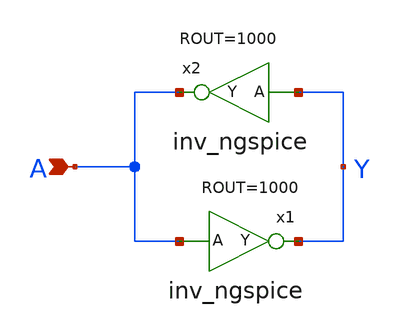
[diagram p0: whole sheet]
** sch_path: xschem_libs_newsym/ngspice/keeper_ngspice/schematic/keeper_ngspice.sch
* Copyright (C) 1998-2024 Stefan Frederik Schippers
* This program is free software; you can redistribute it and/or modify
* it under the terms of the GNU General Public License as published by
* the Free Software Foundation; either version 2 of the License, or
* (at your option) any later version.
* This program is distributed in the hope that it will be useful,
* but WITHOUT ANY WARRANTY; without even the implied warranty of
* MERCHANTABILITY or FITNESS FOR A PARTICULAR PURPOSE.  See the
* GNU General Public License for more details.
* You should have received a copy of the GNU General Public License
* along with this program; if not, write to the Free Software
**.subckt keeper_ngspice A
*.ipin A
x1 Y A inv_ngspice ROUT=1000
x2 A Y inv_ngspice ROUT=1000
**.ends

* expanding   symbol:  ngspice/inv_ngspice.sym # of pins=2
** sym_path: ngspice/inv_ngspice.sym
** sch_path: ngspice/inv_ngspice.sch
.subckt inv_ngspice Y A  ROUT=1000
*.ipin A
*.opin Y
B1 net1 0 V = 'VCC/2*(1-tanh((V(A1)-VCC/2)*100))'
R1 Y1 net1 'ROUT' m=1
C1 A1 0 8f m=1
C2 Y1 0 8f m=1
V1 Y Y1 0
V2 A1 A 0
.ends

.end
